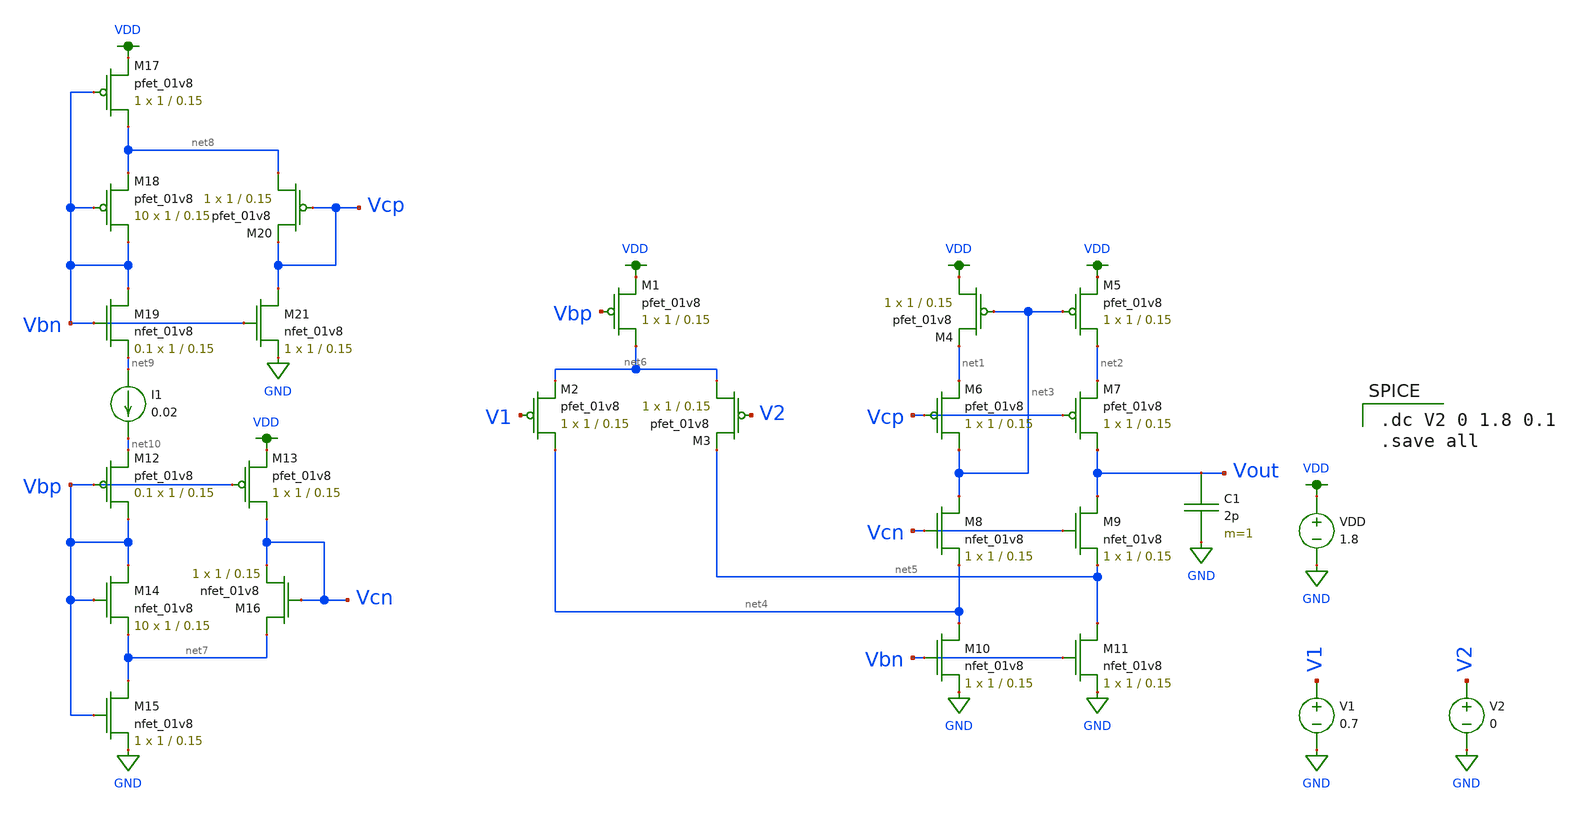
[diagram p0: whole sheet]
** sch_path: schematic/folded_cascode_differential_amplifier.sch
**.subckt folded_cascode_differential_amplifier
XM1 net6 Vbp VDD VDD sky130_fd_pr__pfet_01v8 L=0.15 W=1 nf=1 ad='int((nf+1)/2) * W/nf * 0.29' as='int((nf+2)/2) * W/nf * 0.29'
+ pd='2*int((nf+1)/2) * (W/nf + 0.29)' ps='2*int((nf+2)/2) * (W/nf + 0.29)' nrd='0.29 / W' nrs='0.29 / W'
+ sa=0 sb=0 sd=0 mult=1 m=1
XM2 net4 V1 net6 VDD sky130_fd_pr__pfet_01v8 L=0.15 W=1 nf=1 ad='int((nf+1)/2) * W/nf * 0.29' as='int((nf+2)/2) * W/nf * 0.29'
+ pd='2*int((nf+1)/2) * (W/nf + 0.29)' ps='2*int((nf+2)/2) * (W/nf + 0.29)' nrd='0.29 / W' nrs='0.29 / W'
+ sa=0 sb=0 sd=0 mult=1 m=1
XM3 net6 V2 net5 VDD sky130_fd_pr__pfet_01v8 L=0.15 W=1 nf=1 ad='int((nf+1)/2) * W/nf * 0.29' as='int((nf+2)/2) * W/nf * 0.29'
+ pd='2*int((nf+1)/2) * (W/nf + 0.29)' ps='2*int((nf+2)/2) * (W/nf + 0.29)' nrd='0.29 / W' nrs='0.29 / W'
+ sa=0 sb=0 sd=0 mult=1 m=1
XM4 VDD net3 net1 VDD sky130_fd_pr__pfet_01v8 L=0.15 W=1 nf=1 ad='int((nf+1)/2) * W/nf * 0.29' as='int((nf+2)/2) * W/nf * 0.29'
+ pd='2*int((nf+1)/2) * (W/nf + 0.29)' ps='2*int((nf+2)/2) * (W/nf + 0.29)' nrd='0.29 / W' nrs='0.29 / W'
+ sa=0 sb=0 sd=0 mult=1 m=1
XM5 net2 net3 VDD VDD sky130_fd_pr__pfet_01v8 L=0.15 W=1 nf=1 ad='int((nf+1)/2) * W/nf * 0.29' as='int((nf+2)/2) * W/nf * 0.29'
+ pd='2*int((nf+1)/2) * (W/nf + 0.29)' ps='2*int((nf+2)/2) * (W/nf + 0.29)' nrd='0.29 / W' nrs='0.29 / W'
+ sa=0 sb=0 sd=0 mult=1 m=1
XM6 net3 Vcp net1 VDD sky130_fd_pr__pfet_01v8 L=0.15 W=1 nf=1 ad='int((nf+1)/2) * W/nf * 0.29' as='int((nf+2)/2) * W/nf * 0.29'
+ pd='2*int((nf+1)/2) * (W/nf + 0.29)' ps='2*int((nf+2)/2) * (W/nf + 0.29)' nrd='0.29 / W' nrs='0.29 / W'
+ sa=0 sb=0 sd=0 mult=1 m=1
XM7 Vout Vcp net2 VDD sky130_fd_pr__pfet_01v8 L=0.15 W=1 nf=1 ad='int((nf+1)/2) * W/nf * 0.29' as='int((nf+2)/2) * W/nf * 0.29'
+ pd='2*int((nf+1)/2) * (W/nf + 0.29)' ps='2*int((nf+2)/2) * (W/nf + 0.29)' nrd='0.29 / W' nrs='0.29 / W'
+ sa=0 sb=0 sd=0 mult=1 m=1
XM8 net3 Vcn net4 GND sky130_fd_pr__nfet_01v8 L=0.15 W=1 nf=1 ad='int((nf+1)/2) * W/nf * 0.29' as='int((nf+2)/2) * W/nf * 0.29'
+ pd='2*int((nf+1)/2) * (W/nf + 0.29)' ps='2*int((nf+2)/2) * (W/nf + 0.29)' nrd='0.29 / W' nrs='0.29 / W'
+ sa=0 sb=0 sd=0 mult=1 m=1
XM9 Vout Vcn net5 GND sky130_fd_pr__nfet_01v8 L=0.15 W=1 nf=1 ad='int((nf+1)/2) * W/nf * 0.29' as='int((nf+2)/2) * W/nf * 0.29'
+ pd='2*int((nf+1)/2) * (W/nf + 0.29)' ps='2*int((nf+2)/2) * (W/nf + 0.29)' nrd='0.29 / W' nrs='0.29 / W'
+ sa=0 sb=0 sd=0 mult=1 m=1
XM10 net4 Vbn GND GND sky130_fd_pr__nfet_01v8 L=0.15 W=1 nf=1 ad='int((nf+1)/2) * W/nf * 0.29' as='int((nf+2)/2) * W/nf * 0.29'
+ pd='2*int((nf+1)/2) * (W/nf + 0.29)' ps='2*int((nf+2)/2) * (W/nf + 0.29)' nrd='0.29 / W' nrs='0.29 / W'
+ sa=0 sb=0 sd=0 mult=1 m=1
XM11 net5 Vbn GND GND sky130_fd_pr__nfet_01v8 L=0.15 W=1 nf=1 ad='int((nf+1)/2) * W/nf * 0.29' as='int((nf+2)/2) * W/nf * 0.29'
+ pd='2*int((nf+1)/2) * (W/nf + 0.29)' ps='2*int((nf+2)/2) * (W/nf + 0.29)' nrd='0.29 / W' nrs='0.29 / W'
+ sa=0 sb=0 sd=0 mult=1 m=1
XM12 Vbp Vbp net10 VDD sky130_fd_pr__pfet_01v8 L=0.15 W=1 nf=1 ad='int((nf+1)/2) * W/nf * 0.29' as='int((nf+2)/2) * W/nf * 0.29'
+ pd='2*int((nf+1)/2) * (W/nf + 0.29)' ps='2*int((nf+2)/2) * (W/nf + 0.29)' nrd='0.29 / W' nrs='0.29 / W'
+ sa=0 sb=0 sd=0 mult=0.1 m=0.1
XM13 Vcn Vbp VDD VDD sky130_fd_pr__pfet_01v8 L=0.15 W=1 nf=1 ad='int((nf+1)/2) * W/nf * 0.29' as='int((nf+2)/2) * W/nf * 0.29'
+ pd='2*int((nf+1)/2) * (W/nf + 0.29)' ps='2*int((nf+2)/2) * (W/nf + 0.29)' nrd='0.29 / W' nrs='0.29 / W'
+ sa=0 sb=0 sd=0 mult=1 m=1
XM14 Vbp Vbp net7 GND sky130_fd_pr__nfet_01v8 L=0.15 W=1 nf=1 ad='int((nf+1)/2) * W/nf * 0.29' as='int((nf+2)/2) * W/nf * 0.29'
+ pd='2*int((nf+1)/2) * (W/nf + 0.29)' ps='2*int((nf+2)/2) * (W/nf + 0.29)' nrd='0.29 / W' nrs='0.29 / W'
+ sa=0 sb=0 sd=0 mult=10 m=10
XM15 net7 Vbp GND GND sky130_fd_pr__nfet_01v8 L=0.15 W=1 nf=1 ad='int((nf+1)/2) * W/nf * 0.29' as='int((nf+2)/2) * W/nf * 0.29'
+ pd='2*int((nf+1)/2) * (W/nf + 0.29)' ps='2*int((nf+2)/2) * (W/nf + 0.29)' nrd='0.29 / W' nrs='0.29 / W'
+ sa=0 sb=0 sd=0 mult=1 m=1
XM16 net7 Vcn Vcn GND sky130_fd_pr__nfet_01v8 L=0.15 W=1 nf=1 ad='int((nf+1)/2) * W/nf * 0.29' as='int((nf+2)/2) * W/nf * 0.29'
+ pd='2*int((nf+1)/2) * (W/nf + 0.29)' ps='2*int((nf+2)/2) * (W/nf + 0.29)' nrd='0.29 / W' nrs='0.29 / W'
+ sa=0 sb=0 sd=0 mult=1 m=1
XM17 net8 Vbn VDD VDD sky130_fd_pr__pfet_01v8 L=0.15 W=1 nf=1 ad='int((nf+1)/2) * W/nf * 0.29' as='int((nf+2)/2) * W/nf * 0.29'
+ pd='2*int((nf+1)/2) * (W/nf + 0.29)' ps='2*int((nf+2)/2) * (W/nf + 0.29)' nrd='0.29 / W' nrs='0.29 / W'
+ sa=0 sb=0 sd=0 mult=1 m=1
XM18 Vbn Vbn net8 VDD sky130_fd_pr__pfet_01v8 L=0.15 W=1 nf=1 ad='int((nf+1)/2) * W/nf * 0.29' as='int((nf+2)/2) * W/nf * 0.29'
+ pd='2*int((nf+1)/2) * (W/nf + 0.29)' ps='2*int((nf+2)/2) * (W/nf + 0.29)' nrd='0.29 / W' nrs='0.29 / W'
+ sa=0 sb=0 sd=0 mult=10 m=10
XM19 Vbn Vbn net9 GND sky130_fd_pr__nfet_01v8 L=0.15 W=1 nf=1 ad='int((nf+1)/2) * W/nf * 0.29' as='int((nf+2)/2) * W/nf * 0.29'
+ pd='2*int((nf+1)/2) * (W/nf + 0.29)' ps='2*int((nf+2)/2) * (W/nf + 0.29)' nrd='0.29 / W' nrs='0.29 / W'
+ sa=0 sb=0 sd=0 mult=0.1 m=0.1
XM20 net8 Vcp Vcp VDD sky130_fd_pr__pfet_01v8 L=0.15 W=1 nf=1 ad='int((nf+1)/2) * W/nf * 0.29' as='int((nf+2)/2) * W/nf * 0.29'
+ pd='2*int((nf+1)/2) * (W/nf + 0.29)' ps='2*int((nf+2)/2) * (W/nf + 0.29)' nrd='0.29 / W' nrs='0.29 / W'
+ sa=0 sb=0 sd=0 mult=1 m=1
XM21 Vcp Vbn GND GND sky130_fd_pr__nfet_01v8 L=0.15 W=1 nf=1 ad='int((nf+1)/2) * W/nf * 0.29' as='int((nf+2)/2) * W/nf * 0.29'
+ pd='2*int((nf+1)/2) * (W/nf + 0.29)' ps='2*int((nf+2)/2) * (W/nf + 0.29)' nrd='0.29 / W' nrs='0.29 / W'
+ sa=0 sb=0 sd=0 mult=1 m=1
I1 net9 net10 0.02
VDD VDD GND 1.8
V1 V1 GND 0.7
C1 Vout GND 2p m=1
V2 V2 GND 0
**** begin user architecture code

.option wnflag=1
.lib ~/skywater/skywater-pdk/libraries/sky130_fd_pr_ngspice/latest/models/sky130.lib.spice tt


.dc V2 0 1.8 0.1
.save all

**** end user architecture code
**.ends
.GLOBAL VDD
.GLOBAL GND
.end
